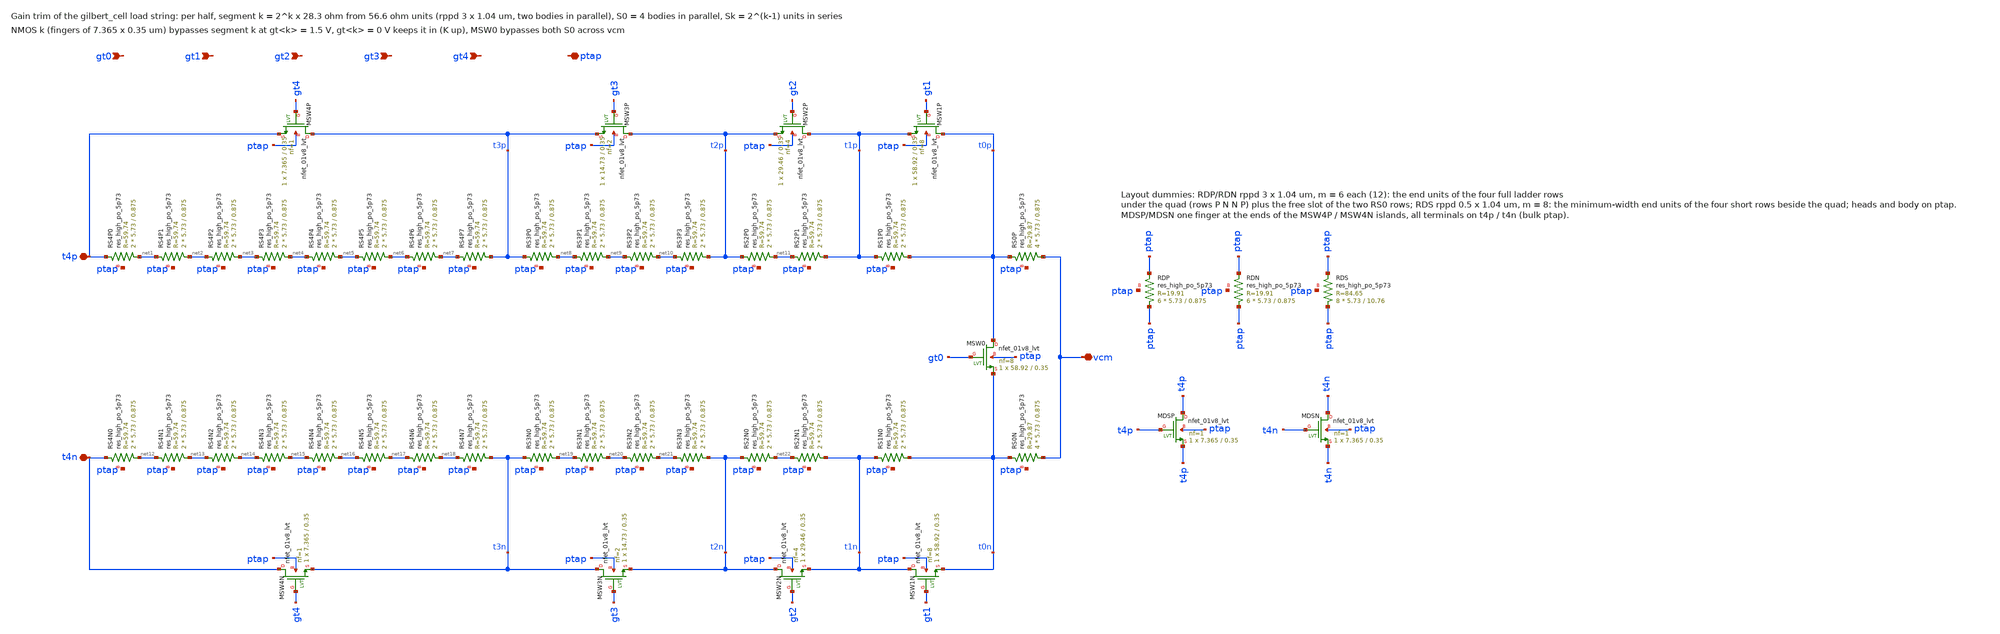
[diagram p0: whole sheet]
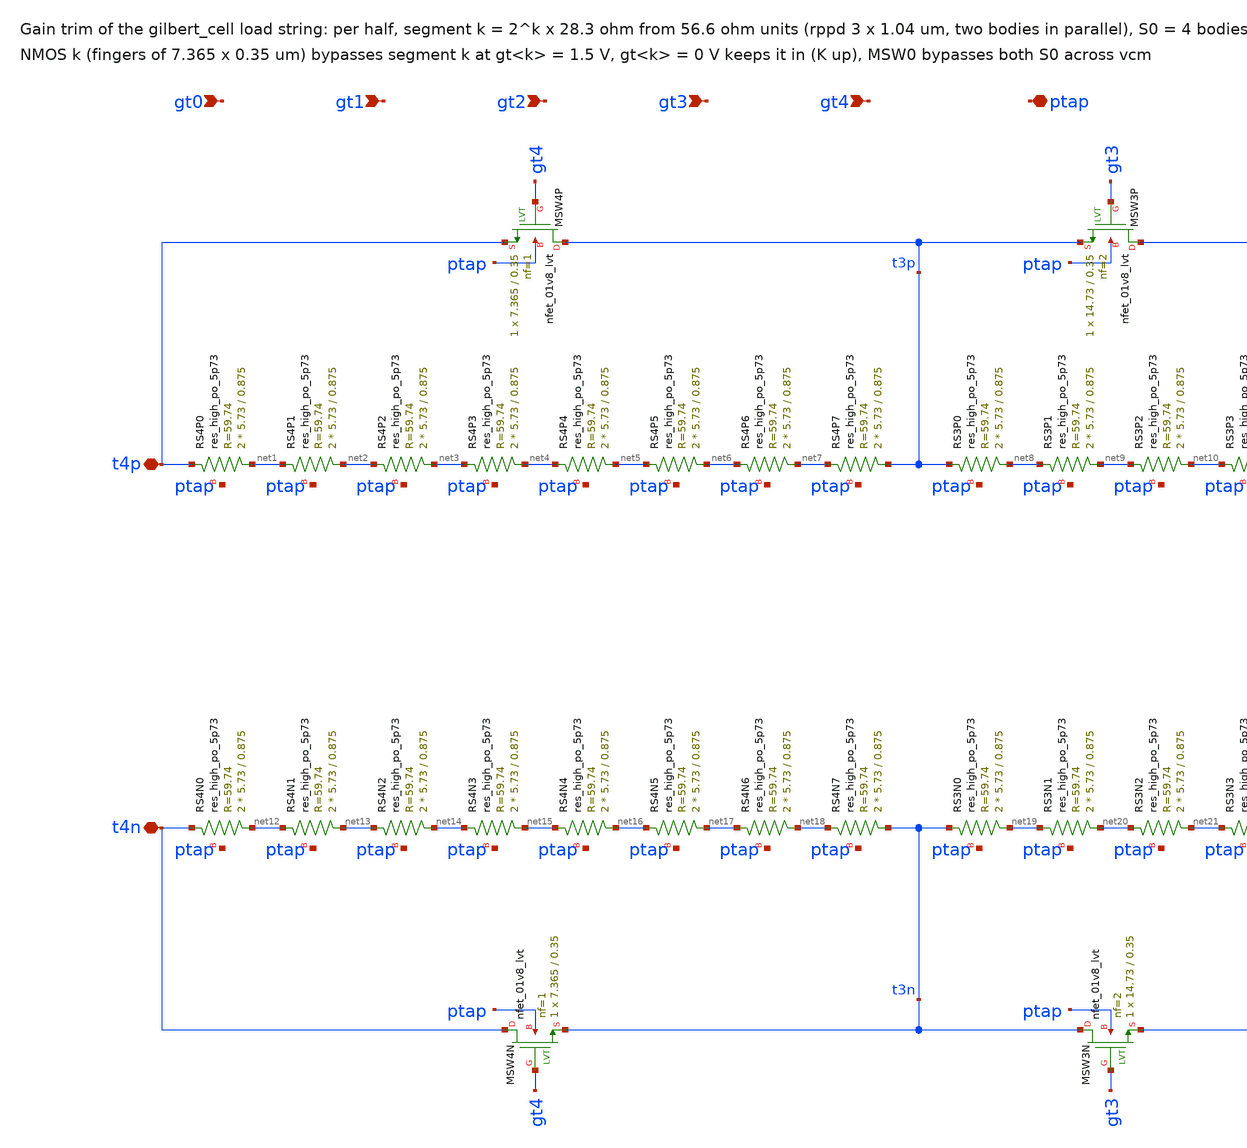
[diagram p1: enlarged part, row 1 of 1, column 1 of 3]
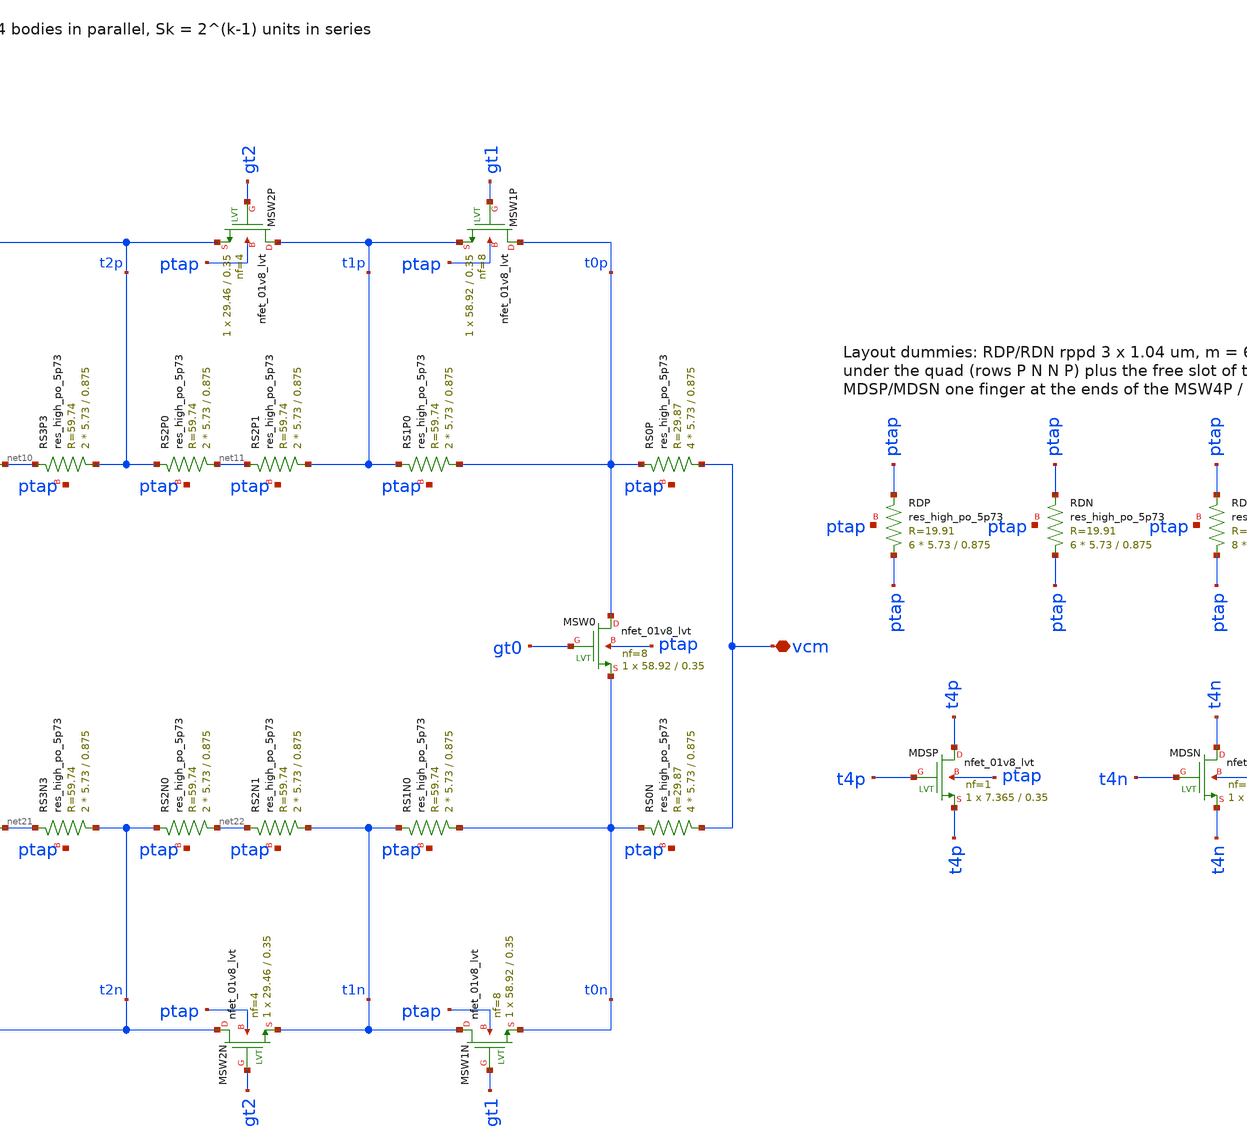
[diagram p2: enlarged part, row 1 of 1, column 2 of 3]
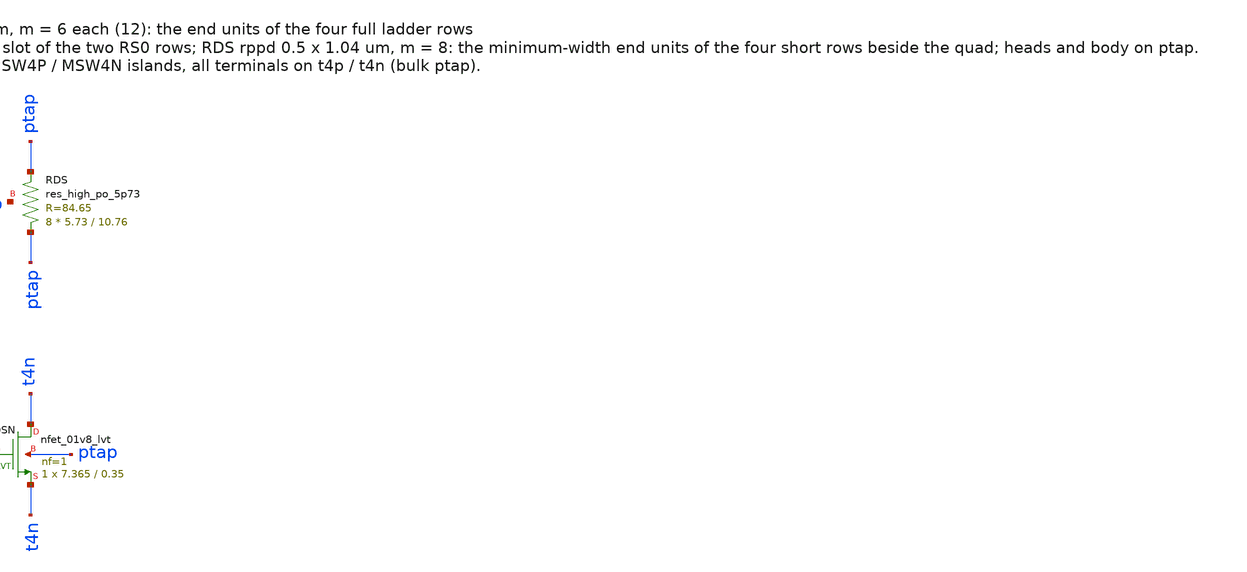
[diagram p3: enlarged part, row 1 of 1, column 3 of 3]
** sch_path: macros/gilbert_cell/schematic/xschem/gain_trim.sch
**.subckt gain_trim t4p t4n vcm gt0 gt1 gt2 gt3 gt4 ptap
*.iopin t4p
*.iopin t4n
*.iopin vcm
*.ipin gt0
*.ipin gt1
*.ipin gt2
*.ipin gt3
*.ipin gt4
*.iopin ptap
XRS4P0 net1 t4p ptap sky130_fd_pr__res_high_po_5p73 L=0.875 mult=2 m=2
XRS4P1 net2 net1 ptap sky130_fd_pr__res_high_po_5p73 L=0.875 mult=2 m=2
XRS4P2 net3 net2 ptap sky130_fd_pr__res_high_po_5p73 L=0.875 mult=2 m=2
XRS4P3 net4 net3 ptap sky130_fd_pr__res_high_po_5p73 L=0.875 mult=2 m=2
XRS4P4 net5 net4 ptap sky130_fd_pr__res_high_po_5p73 L=0.875 mult=2 m=2
XRS4P5 net6 net5 ptap sky130_fd_pr__res_high_po_5p73 L=0.875 mult=2 m=2
XRS4P6 net7 net6 ptap sky130_fd_pr__res_high_po_5p73 L=0.875 mult=2 m=2
XRS4P7 t3p net7 ptap sky130_fd_pr__res_high_po_5p73 L=0.875 mult=2 m=2
XRS3P0 net8 t3p ptap sky130_fd_pr__res_high_po_5p73 L=0.875 mult=2 m=2
XRS3P1 net9 net8 ptap sky130_fd_pr__res_high_po_5p73 L=0.875 mult=2 m=2
XRS3P2 net10 net9 ptap sky130_fd_pr__res_high_po_5p73 L=0.875 mult=2 m=2
XRS3P3 t2p net10 ptap sky130_fd_pr__res_high_po_5p73 L=0.875 mult=2 m=2
XRS2P0 net11 t2p ptap sky130_fd_pr__res_high_po_5p73 L=0.875 mult=2 m=2
XRS2P1 t1p net11 ptap sky130_fd_pr__res_high_po_5p73 L=0.875 mult=2 m=2
XRS1P0 t0p t1p ptap sky130_fd_pr__res_high_po_5p73 L=0.875 mult=2 m=2
XRS0P vcm t0p ptap sky130_fd_pr__res_high_po_5p73 L=0.875 mult=4 m=4
XMSW4P t3p gt4 t4p ptap sky130_fd_pr__nfet_01v8_lvt L=0.35 W=7.365 nf=1 ad='int((1 + 1)/2) * 7.365 / 1 * 0.29'
+ as='int((1 + 2)/2) * 7.365 / 1 * 0.29' pd='2*int((1 + 1)/2) * (7.365 / 1 + 0.29)' ps='2*int((1 + 2)/2) * (7.365 / 1 + 0.29)'
+ nrd='0.29 / 7.365 ' nrs='0.29 / 7.365 ' sa=0 sb=0 sd=0 mult=1 m=1
XMSW3P t2p gt3 t3p ptap sky130_fd_pr__nfet_01v8_lvt L=0.35 W=14.73 nf=2 ad='int((2 + 1)/2) * 14.73 / 2 * 0.29'
+ as='int((2 + 2)/2) * 14.73 / 2 * 0.29' pd='2*int((2 + 1)/2) * (14.73 / 2 + 0.29)' ps='2*int((2 + 2)/2) * (14.73 / 2 + 0.29)'
+ nrd='0.29 / 14.73 ' nrs='0.29 / 14.73 ' sa=0 sb=0 sd=0 mult=1 m=1
XMSW2P t1p gt2 t2p ptap sky130_fd_pr__nfet_01v8_lvt L=0.35 W=29.46 nf=4 ad='int((4 + 1)/2) * 29.46 / 4 * 0.29'
+ as='int((4 + 2)/2) * 29.46 / 4 * 0.29' pd='2*int((4 + 1)/2) * (29.46 / 4 + 0.29)' ps='2*int((4 + 2)/2) * (29.46 / 4 + 0.29)'
+ nrd='0.29 / 29.46 ' nrs='0.29 / 29.46 ' sa=0 sb=0 sd=0 mult=1 m=1
XMSW1P t0p gt1 t1p ptap sky130_fd_pr__nfet_01v8_lvt L=0.35 W=58.92 nf=8 ad='int((8 + 1)/2) * 58.92 / 8 * 0.29'
+ as='int((8 + 2)/2) * 58.92 / 8 * 0.29' pd='2*int((8 + 1)/2) * (58.92 / 8 + 0.29)' ps='2*int((8 + 2)/2) * (58.92 / 8 + 0.29)'
+ nrd='0.29 / 58.92 ' nrs='0.29 / 58.92 ' sa=0 sb=0 sd=0 mult=1 m=1
XRS4N0 net12 t4n ptap sky130_fd_pr__res_high_po_5p73 L=0.875 mult=2 m=2
XRS4N1 net13 net12 ptap sky130_fd_pr__res_high_po_5p73 L=0.875 mult=2 m=2
XRS4N2 net14 net13 ptap sky130_fd_pr__res_high_po_5p73 L=0.875 mult=2 m=2
XRS4N3 net15 net14 ptap sky130_fd_pr__res_high_po_5p73 L=0.875 mult=2 m=2
XRS4N4 net16 net15 ptap sky130_fd_pr__res_high_po_5p73 L=0.875 mult=2 m=2
XRS4N5 net17 net16 ptap sky130_fd_pr__res_high_po_5p73 L=0.875 mult=2 m=2
XRS4N6 net18 net17 ptap sky130_fd_pr__res_high_po_5p73 L=0.875 mult=2 m=2
XRS4N7 t3n net18 ptap sky130_fd_pr__res_high_po_5p73 L=0.875 mult=2 m=2
XRS3N0 net19 t3n ptap sky130_fd_pr__res_high_po_5p73 L=0.875 mult=2 m=2
XRS3N1 net20 net19 ptap sky130_fd_pr__res_high_po_5p73 L=0.875 mult=2 m=2
XRS3N2 net21 net20 ptap sky130_fd_pr__res_high_po_5p73 L=0.875 mult=2 m=2
XRS3N3 t2n net21 ptap sky130_fd_pr__res_high_po_5p73 L=0.875 mult=2 m=2
XRS2N0 net22 t2n ptap sky130_fd_pr__res_high_po_5p73 L=0.875 mult=2 m=2
XRS2N1 t1n net22 ptap sky130_fd_pr__res_high_po_5p73 L=0.875 mult=2 m=2
XRS1N0 t0n t1n ptap sky130_fd_pr__res_high_po_5p73 L=0.875 mult=2 m=2
XRS0N vcm t0n ptap sky130_fd_pr__res_high_po_5p73 L=0.875 mult=4 m=4
XMSW4N t4n gt4 t3n ptap sky130_fd_pr__nfet_01v8_lvt L=0.35 W=7.365 nf=1 ad='int((1 + 1)/2) * 7.365 / 1 * 0.29'
+ as='int((1 + 2)/2) * 7.365 / 1 * 0.29' pd='2*int((1 + 1)/2) * (7.365 / 1 + 0.29)' ps='2*int((1 + 2)/2) * (7.365 / 1 + 0.29)'
+ nrd='0.29 / 7.365 ' nrs='0.29 / 7.365 ' sa=0 sb=0 sd=0 mult=1 m=1
XMSW3N t3n gt3 t2n ptap sky130_fd_pr__nfet_01v8_lvt L=0.35 W=14.73 nf=2 ad='int((2 + 1)/2) * 14.73 / 2 * 0.29'
+ as='int((2 + 2)/2) * 14.73 / 2 * 0.29' pd='2*int((2 + 1)/2) * (14.73 / 2 + 0.29)' ps='2*int((2 + 2)/2) * (14.73 / 2 + 0.29)'
+ nrd='0.29 / 14.73 ' nrs='0.29 / 14.73 ' sa=0 sb=0 sd=0 mult=1 m=1
XMSW2N t2n gt2 t1n ptap sky130_fd_pr__nfet_01v8_lvt L=0.35 W=29.46 nf=4 ad='int((4 + 1)/2) * 29.46 / 4 * 0.29'
+ as='int((4 + 2)/2) * 29.46 / 4 * 0.29' pd='2*int((4 + 1)/2) * (29.46 / 4 + 0.29)' ps='2*int((4 + 2)/2) * (29.46 / 4 + 0.29)'
+ nrd='0.29 / 29.46 ' nrs='0.29 / 29.46 ' sa=0 sb=0 sd=0 mult=1 m=1
XMSW1N t1n gt1 t0n ptap sky130_fd_pr__nfet_01v8_lvt L=0.35 W=58.92 nf=8 ad='int((8 + 1)/2) * 58.92 / 8 * 0.29'
+ as='int((8 + 2)/2) * 58.92 / 8 * 0.29' pd='2*int((8 + 1)/2) * (58.92 / 8 + 0.29)' ps='2*int((8 + 2)/2) * (58.92 / 8 + 0.29)'
+ nrd='0.29 / 58.92 ' nrs='0.29 / 58.92 ' sa=0 sb=0 sd=0 mult=1 m=1
XMSW0 t0p gt0 t0n ptap sky130_fd_pr__nfet_01v8_lvt L=0.35 W=58.92 nf=8 ad='int((8 + 1)/2) * 58.92 / 8 * 0.29'
+ as='int((8 + 2)/2) * 58.92 / 8 * 0.29' pd='2*int((8 + 1)/2) * (58.92 / 8 + 0.29)' ps='2*int((8 + 2)/2) * (58.92 / 8 + 0.29)'
+ nrd='0.29 / 58.92 ' nrs='0.29 / 58.92 ' sa=0 sb=0 sd=0 mult=1 m=1
XRDP ptap ptap ptap sky130_fd_pr__res_high_po_5p73 L=0.875 mult=6 m=6
XRDN ptap ptap ptap sky130_fd_pr__res_high_po_5p73 L=0.875 mult=6 m=6
XRDS ptap ptap ptap sky130_fd_pr__res_high_po_5p73 L=10.76 mult=8 m=8
XMDSP t4p t4p t4p ptap sky130_fd_pr__nfet_01v8_lvt L=0.35 W=7.365 nf=1 ad='int((1 + 1)/2) * 7.365 / 1 * 0.29'
+ as='int((1 + 2)/2) * 7.365 / 1 * 0.29' pd='2*int((1 + 1)/2) * (7.365 / 1 + 0.29)' ps='2*int((1 + 2)/2) * (7.365 / 1 + 0.29)'
+ nrd='0.29 / 7.365 ' nrs='0.29 / 7.365 ' sa=0 sb=0 sd=0 mult=1 m=1
XMDSN t4n t4n t4n ptap sky130_fd_pr__nfet_01v8_lvt L=0.35 W=7.365 nf=1 ad='int((1 + 1)/2) * 7.365 / 1 * 0.29'
+ as='int((1 + 2)/2) * 7.365 / 1 * 0.29' pd='2*int((1 + 1)/2) * (7.365 / 1 + 0.29)' ps='2*int((1 + 2)/2) * (7.365 / 1 + 0.29)'
+ nrd='0.29 / 7.365 ' nrs='0.29 / 7.365 ' sa=0 sb=0 sd=0 mult=1 m=1
**.ends
.end
